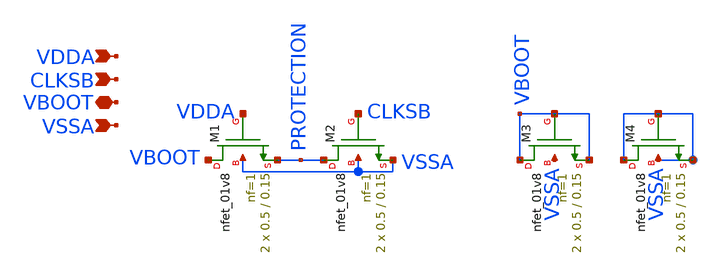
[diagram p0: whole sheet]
** sch_path: xschem/ncell_bsw_dischrg.sch
**.subckt ncell_bsw_dischrg VDDA CLKSB VBOOT VSSA
*.ipin VDDA
*.ipin CLKSB
*.iopin VBOOT
*.ipin VSSA
XM1 VBOOT VDDA PROTECTION VSSA sky130_fd_pr__nfet_01v8 L=0.15 W=0.5 nf=1 ad='int((nf+1)/2) * W/nf * 0.29'
+ as='int((nf+2)/2) * W/nf * 0.29' pd='2*int((nf+1)/2) * (W/nf + 0.29)' ps='2*int((nf+2)/2) * (W/nf + 0.29)'
+ nrd='0.29 / W' nrs='0.29 / W' sa=0 sb=0 sd=0 mult=2 m=2
XM2 PROTECTION CLKSB VSSA VSSA sky130_fd_pr__nfet_01v8 L=0.15 W=0.5 nf=1 ad='int((nf+1)/2) * W/nf * 0.29'
+ as='int((nf+2)/2) * W/nf * 0.29' pd='2*int((nf+1)/2) * (W/nf + 0.29)' ps='2*int((nf+2)/2) * (W/nf + 0.29)'
+ nrd='0.29 / W' nrs='0.29 / W' sa=0 sb=0 sd=0 mult=2 m=2
XM3 VBOOT VBOOT VBOOT VSSA sky130_fd_pr__nfet_01v8 L=0.15 W=0.5 nf=1 ad='int((nf+1)/2) * W/nf * 0.29'
+ as='int((nf+2)/2) * W/nf * 0.29' pd='2*int((nf+1)/2) * (W/nf + 0.29)' ps='2*int((nf+2)/2) * (W/nf + 0.29)'
+ nrd='0.29 / W' nrs='0.29 / W' sa=0 sb=0 sd=0 mult=2 m=2
XM4 VSSA VSSA VSSA VSSA sky130_fd_pr__nfet_01v8 L=0.15 W=0.5 nf=1 ad='int((nf+1)/2) * W/nf * 0.29' as='int((nf+2)/2) * W/nf * 0.29'
+ pd='2*int((nf+1)/2) * (W/nf + 0.29)' ps='2*int((nf+2)/2) * (W/nf + 0.29)' nrd='0.29 / W' nrs='0.29 / W'
+ sa=0 sb=0 sd=0 mult=2 m=2
**.ends
.end
